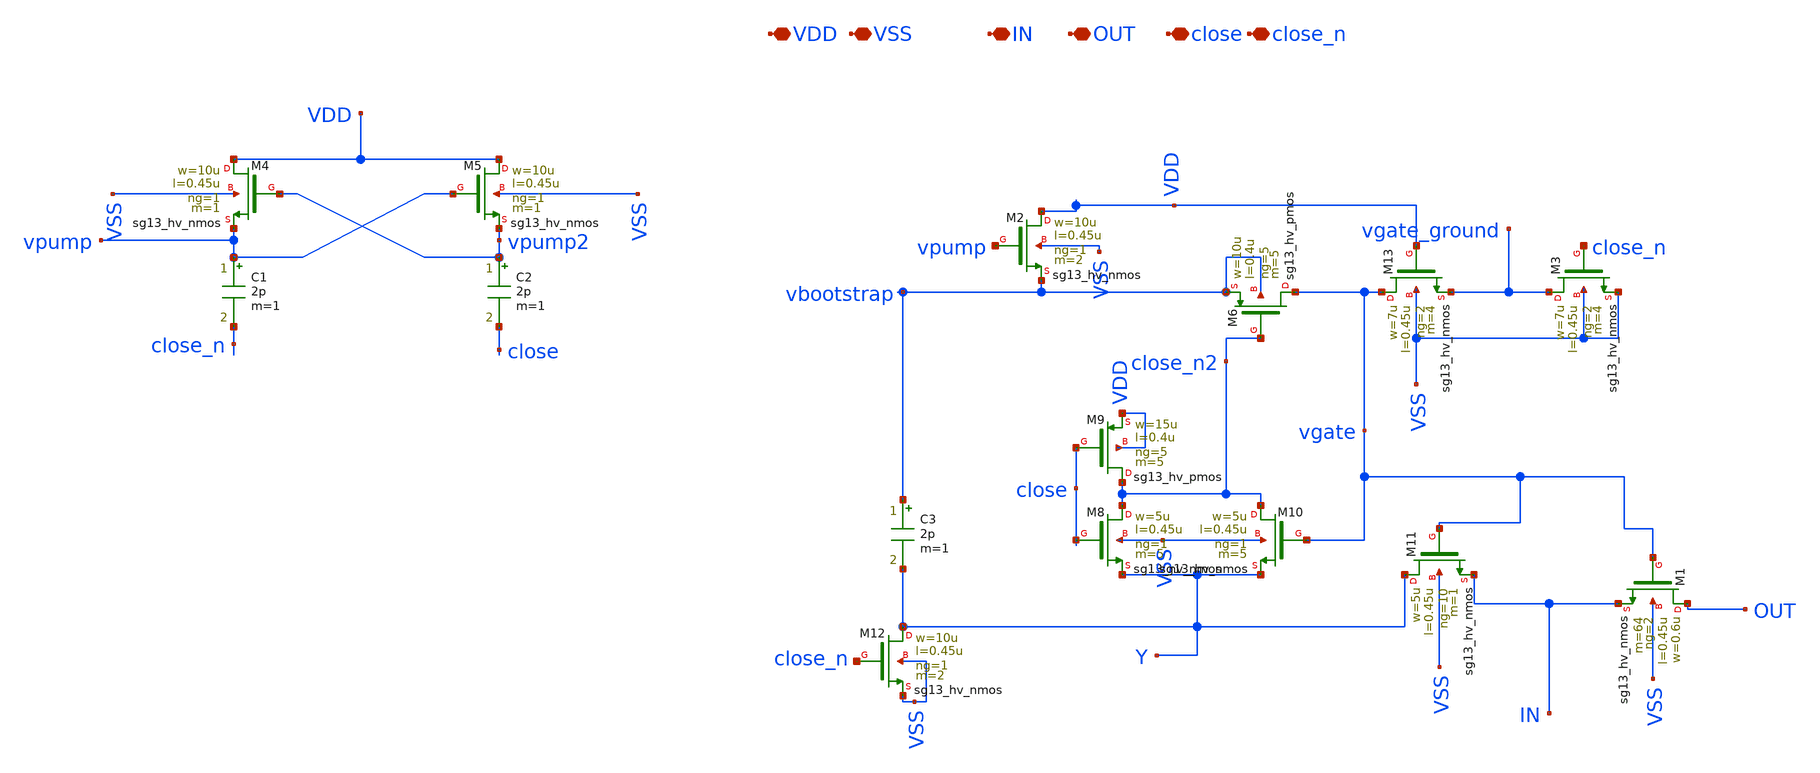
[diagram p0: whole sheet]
** sch_path: xschem/bootstrap/bootstrap.sch
**.subckt bootstrap VDD VSS IN OUT close close_n
*.iopin VDD
*.iopin VSS
*.iopin IN
*.iopin OUT
*.iopin close
*.iopin close_n
C1 vpump close_n 2p m=1
C2 vpump2 close 2p m=1
XM6 vgate close_n2 vbootstrap vbootstrap sg13_hv_pmos w=10u l=0.4u ng=5 m=5 mm_ok=1
XM8 close_n2 close Y VSS sg13_hv_nmos w=5u l=0.45u ng=1 m=5 mm_ok=1
XM9 close_n2 close VDD VDD sg13_hv_pmos w=15u l=0.4u ng=5 m=5 mm_ok=1
XM10 close_n2 vgate Y VSS sg13_hv_nmos w=5u l=0.45u ng=1 m=5 mm_ok=1
XM11 Y vgate IN VSS sg13_hv_nmos w=5u l=0.45u ng=10 m=1 mm_ok=1
C3 vbootstrap Y 2p m=1
XM12 Y close_n VSS VSS sg13_hv_nmos w=10u l=0.45u ng=1 m=2 mm_ok=1
XM13 vgate VDD vgate_ground VSS sg13_hv_nmos w=7u l=0.45u ng=2 m=4 mm_ok=1
XM3 vgate_ground close_n VSS VSS sg13_hv_nmos w=7u l=0.45u ng=2 m=4 mm_ok=1
XM4 VDD vpump2 vpump VSS sg13_hv_nmos w=10u l=0.45u ng=1 m=1 mm_ok=1
XM5 VDD vpump vpump2 VSS sg13_hv_nmos w=10u l=0.45u ng=1 m=1 mm_ok=1
XM1 OUT vgate IN VSS sg13_hv_nmos w=0.6u l=0.45u ng=2 m=64 mm_ok=1
XM2 VDD vpump vbootstrap VSS sg13_hv_nmos w=10u l=0.45u ng=1 m=2 mm_ok=1
**.ends
.end
